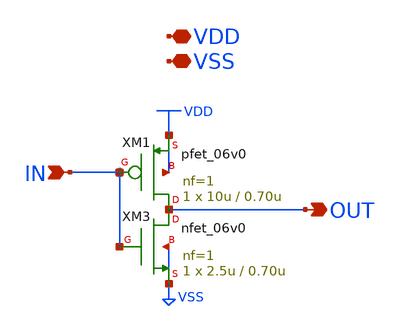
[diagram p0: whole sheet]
** sch_path: io_inv_2i.sch
* Copyright 2023 David Mitchell Bailey
* Licensed under the Apache License, Version 2.0 (the "License");
* you may not use this file except in compliance with the License.
* You may obtain a copy of the License at
* https://www.apache.org/licenses/LICENSE-2.0
* Unless required by applicable law or agreed to in writing, software
* distributed under the License is distributed on an "AS IS" BASIS,
* WITHOUT WARRANTIES OR CONDITIONS OF ANY KIND, either express or implied.
* See the License for the specific language governing permissions and
* limitations under the License.
**.subckt io_inv_2i OUT IN VDD VSS
*.opin OUT
*.ipin IN
*.iopin VDD
*.iopin VSS
XM1 OUT IN VDD VDD pfet_06v0 L=0.70u W=10u nf=1 ad='int((nf+1)/2) * W/nf * 0.18u' as='int((nf+2)/2) * W/nf * 0.18u'
+ pd='2*int((nf+1)/2) * (W/nf + 0.18u)' ps='2*int((nf+2)/2) * (W/nf + 0.18u)' nrd='0.18u / W' nrs='0.18u / W'
+ sa=0 sb=0 sd=0 m=1
XM3 OUT IN VSS VSS nfet_06v0 L=0.70u W=2.5u nf=1 ad='int((nf+1)/2) * W/nf * 0.18u' as='int((nf+2)/2) * W/nf * 0.18u'
+ pd='2*int((nf+1)/2) * (W/nf + 0.18u)' ps='2*int((nf+2)/2) * (W/nf + 0.18u)' nrd='0.18u / W' nrs='0.18u / W'
+ sa=0 sb=0 sd=0 m=1
**.ends
.GLOBAL VDD
.end
